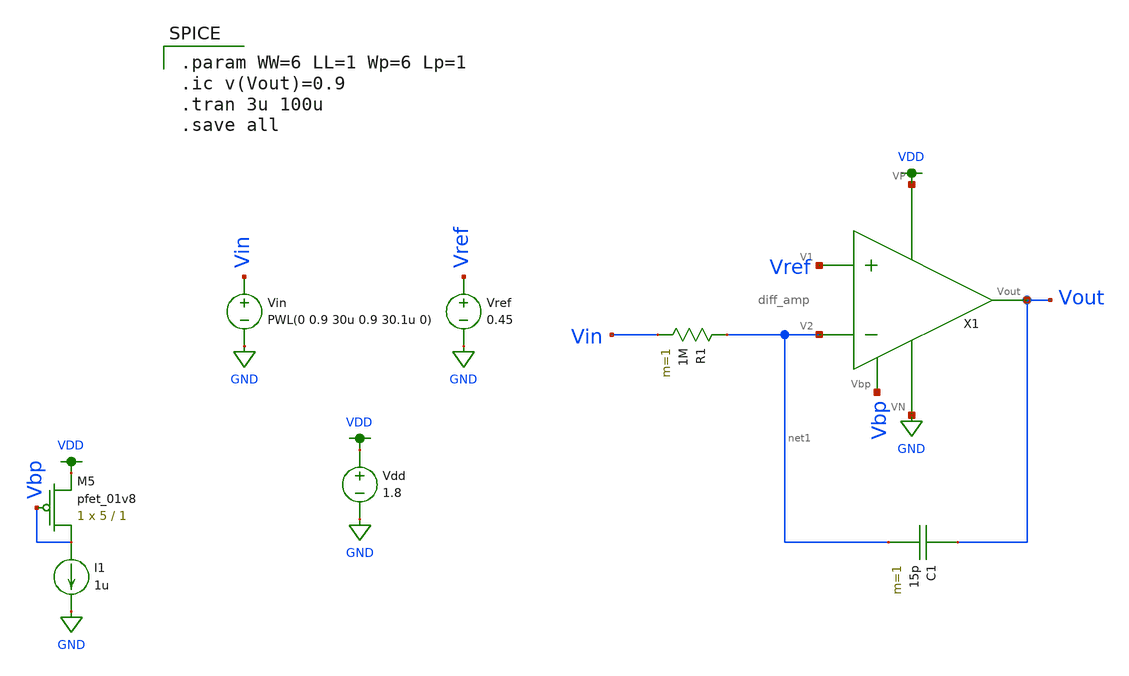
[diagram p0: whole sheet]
** sch_path: schematic/fg_integrator_test.sch
**.subckt fg_integrator_test
Vdd VDD GND 1.8
XM5 Vbp Vbp VDD VDD sky130_fd_pr__pfet_01v8 L=1 W=5 nf=1 ad='int((nf+1)/2) * W/nf * 0.29' as='int((nf+2)/2) * W/nf * 0.29'
+ pd='2*int((nf+1)/2) * (W/nf + 0.29)' ps='2*int((nf+2)/2) * (W/nf + 0.29)' nrd='0.29 / W' nrs='0.29 / W'
+ sa=0 sb=0 sd=0 mult=1 m=1
I1 Vbp GND 1u
C1 Vout net1 15p m=1
Vin Vin GND PWL(0 0.9 30u 0.9 30.1u 0)
X1 VDD Vbp Vout Vref net1 GND diff_amp
R1 net1 Vin 1M m=1
Vref Vref GND 0.45
**** begin user architecture code

.param WW=6 LL=1 Wp=6 Lp=1
.ic v(Vout)=0.9
.tran 3u 100u
.save all


.option wnflag=1
.param MC_SWITCH=0.0
.lib ~/skywater/skywater-pdk/libraries/sky130_fd_pr_ngspice/latest/models/sky130.lib.spice tt

**** end user architecture code
**.ends
.GLOBAL GND
.GLOBAL VDD
.end
